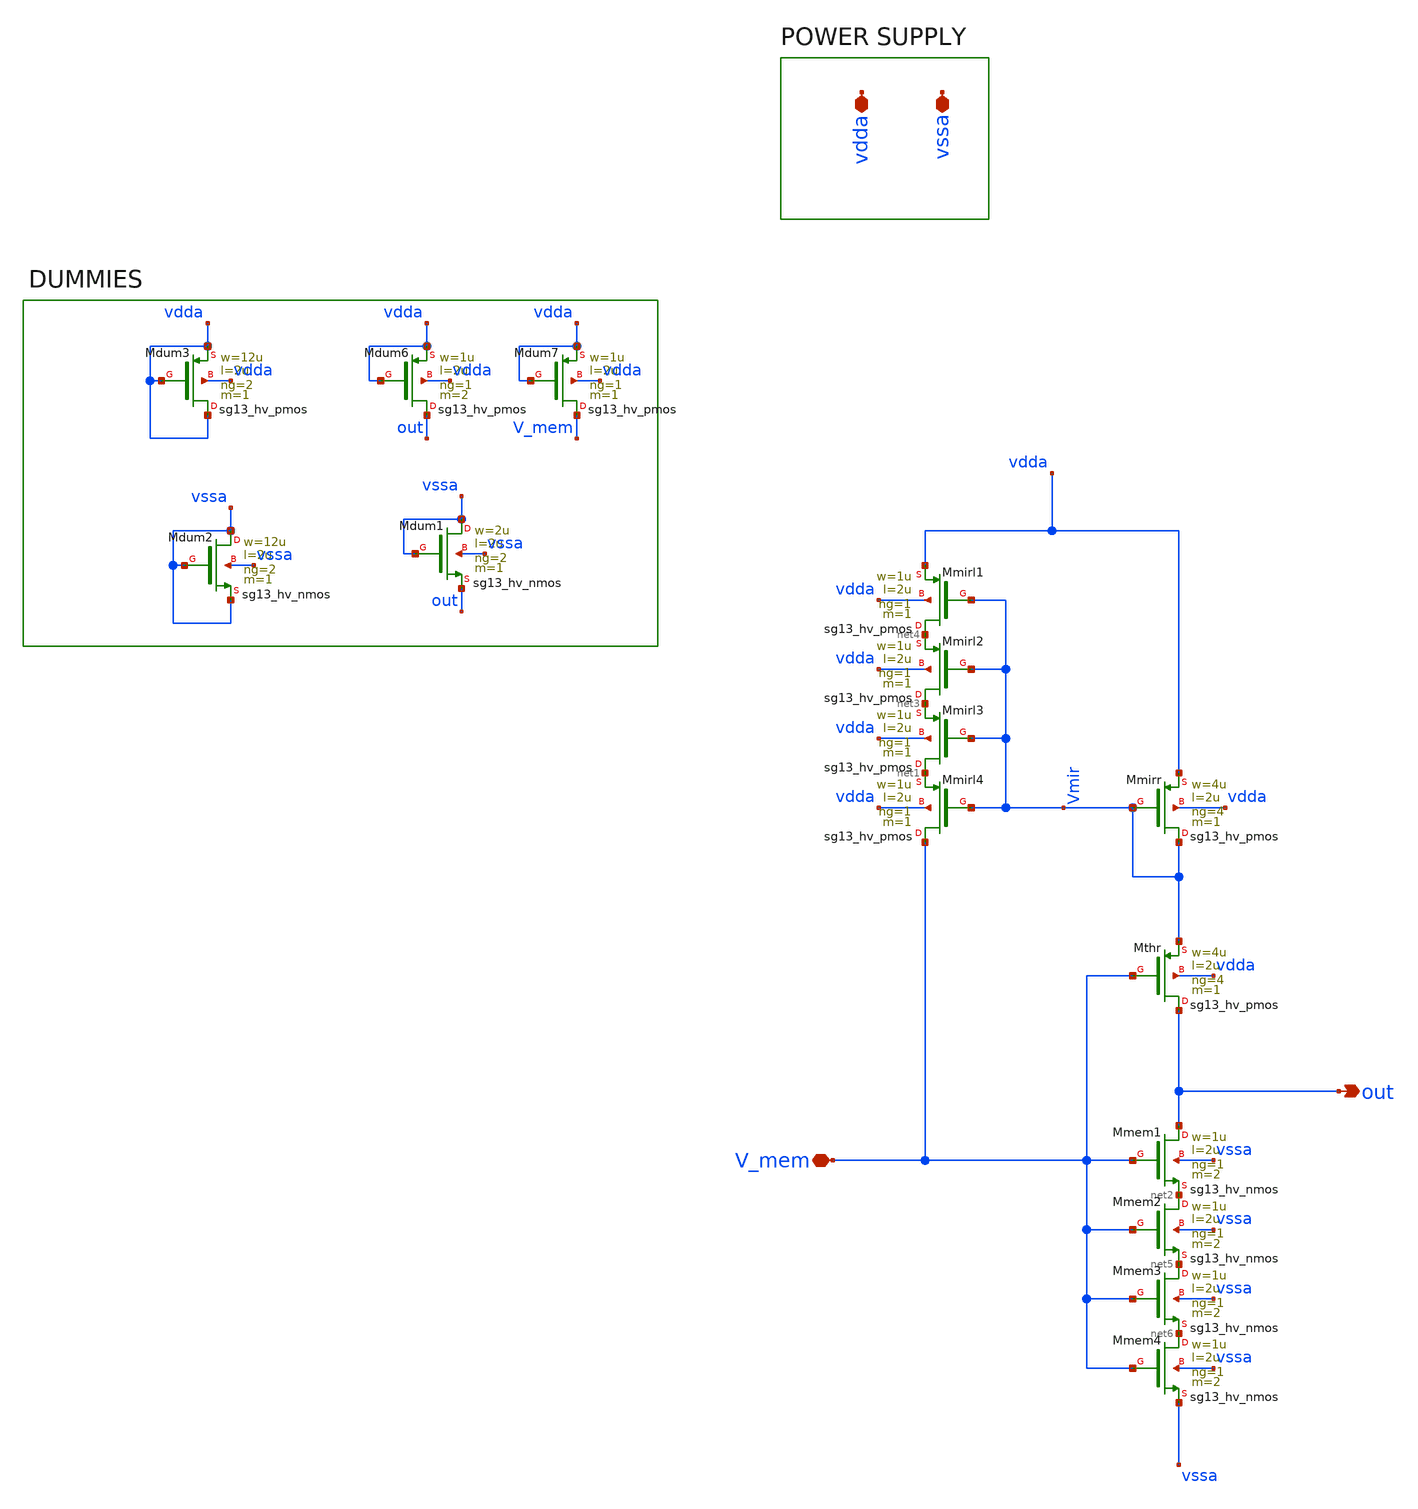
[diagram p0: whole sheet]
** sch_path: FB_system.sch
**.subckt FB_system out V_mem vssa vdda
*.opin out
*.iopin V_mem
*.iopin vssa
*.iopin vdda
XMmirr Vmir Vmir vdda vdda sg13_hv_pmos w=4u l=2u ng=4 m=1 mm_ok=1
XMmirl4 V_mem Vmir net1 vdda sg13_hv_pmos w=1u l=2u ng=1 m=1 mm_ok=1
XMthr out V_mem Vmir vdda sg13_hv_pmos w=4u l=2u ng=4 m=1 mm_ok=1
XMmem1 out V_mem net2 vssa sg13_hv_nmos w=1u l=2u ng=1 m=2 mm_ok=1
XMmirl3 net1 Vmir net3 vdda sg13_hv_pmos w=1u l=2u ng=1 m=1 mm_ok=1
XMmirl2 net3 Vmir net4 vdda sg13_hv_pmos w=1u l=2u ng=1 m=1 mm_ok=1
XMmirl1 net4 Vmir vdda vdda sg13_hv_pmos w=1u l=2u ng=1 m=1 mm_ok=1
XMmem2 net2 V_mem net5 vssa sg13_hv_nmos w=1u l=2u ng=1 m=2 mm_ok=1
XMmem3 net5 V_mem net6 vssa sg13_hv_nmos w=1u l=2u ng=1 m=2 mm_ok=1
XMmem4 net6 V_mem vssa vssa sg13_hv_nmos w=1u l=2u ng=1 m=2 mm_ok=1
XMdum6 out vdda vdda vdda sg13_hv_pmos w=1u l=2u ng=1 m=2 mm_ok=1
XMdum7 V_mem vdda vdda vdda sg13_hv_pmos w=1u l=2u ng=1 m=1 mm_ok=1
XMdum1 vssa vssa out vssa sg13_hv_nmos w=2u l=2u ng=2 m=1 mm_ok=1
XMdum2 vssa vssa vssa vssa sg13_hv_nmos w=12u l=2u ng=2 m=1 mm_ok=1
XMdum3 vdda vdda vdda vdda sg13_hv_pmos w=12u l=2u ng=2 m=1 mm_ok=1
**.ends
.end
